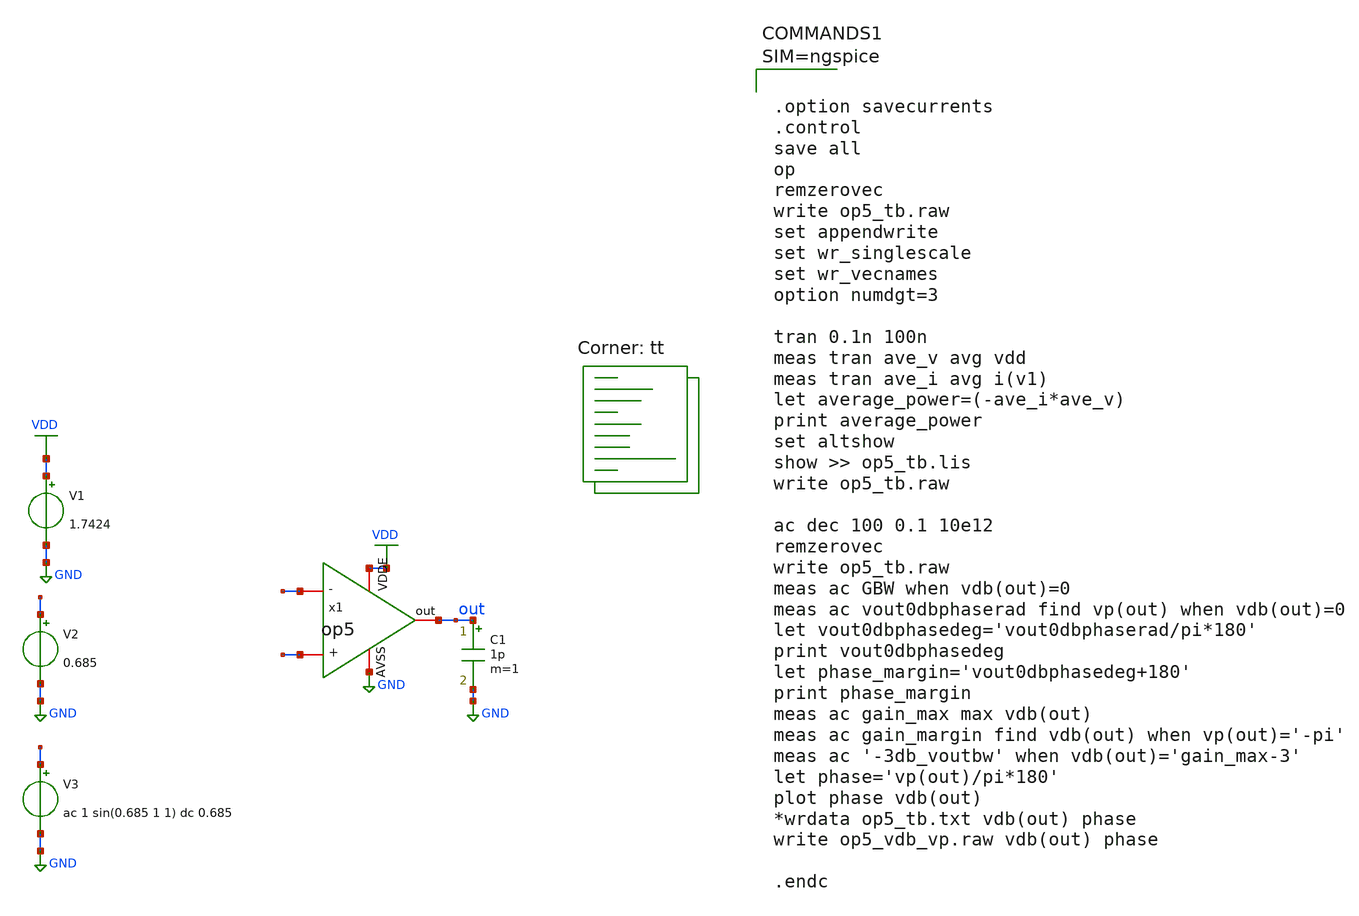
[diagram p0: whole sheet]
** sch_path: xschem/op5_tb.sch
**.subckt op5_tb
V1 VDD GND 1.7424
V2 - GND 0.685
V3 + GND ac 1 sin(0.685 1 1) dc 0.685
C1 out GND 1p m=1
x1 out VDD GND + - op5
**** begin user architecture code



.option savecurrents
.control
save all
op
remzerovec
write op5_tb.raw
set appendwrite
set wr_singlescale
set wr_vecnames
option numdgt=3

tran 0.1n 100n
meas tran ave_v avg vdd
meas tran ave_i avg i(v1)
let average_power=(-ave_i*ave_v)
print average_power
set altshow
show >> op5_tb.lis
write op5_tb.raw

ac dec 100 0.1 10e12
remzerovec
write op5_tb.raw
meas ac GBW when vdb(out)=0
meas ac vout0dbphaserad find vp(out) when vdb(out)=0
let vout0dbphasedeg='vout0dbphaserad/pi*180'
print vout0dbphasedeg
let phase_margin='vout0dbphasedeg+180'
print phase_margin
meas ac gain_max max vdb(out)
meas ac gain_margin find vdb(out) when vp(out)='-pi'
meas ac '-3db_voutbw' when vdb(out)='gain_max-3'
let phase='vp(out)/pi*180'
plot phase vdb(out)
*wrdata op5_tb.txt vdb(out) phase
write op5_vdb_vp.raw vdb(out) phase

.endc



.lib $::SKYWATER_MODELS/sky130.lib.spice tt
**** end user architecture code
**.ends

* expanding   symbol:  op5.sym # of pins=5
** sym_path: xschem/op5.sym
** sch_path: xschem/op5.sch
.subckt op5 out VDDE AVSS + -
*.iopin AVSS
*.iopin -
*.iopin +
*.iopin VDDE
*.iopin out
XM8 net1 net2 VDDE vdde sky130_fd_pr__pfet_01v8 L={L7} W={W7} nf=1 ad='int((nf+1)/2) * W/nf * 0.29' as='int((nf+2)/2) * W/nf * 0.29'
+ pd='2*int((nf+1)/2) * (W/nf + 0.29)' ps='2*int((nf+2)/2) * (W/nf + 0.29)' nrd='0.29 / W' nrs='0.29 / W'
+ sa=0 sb=0 sd=0 mult=2 m=2
XM9 net2 net2 VDDE vdde sky130_fd_pr__pfet_01v8 L={L7} W={W7} nf=1 ad='int((nf+1)/2) * W/nf * 0.29' as='int((nf+2)/2) * W/nf * 0.29'
+ pd='2*int((nf+1)/2) * (W/nf + 0.29)' ps='2*int((nf+2)/2) * (W/nf + 0.29)' nrd='0.29 / W' nrs='0.29 / W'
+ sa=0 sb=0 sd=0 mult=2 m=2
XM5 net3 bias AVSS AVSS sky130_fd_pr__nfet_01v8 L={L6} W={W6} nf=1 ad='int((nf+1)/2) * W/nf * 0.29' as='int((nf+2)/2) * W/nf * 0.29'
+ pd='2*int((nf+1)/2) * (W/nf + 0.29)' ps='2*int((nf+2)/2) * (W/nf + 0.29)' nrd='0.29 / W' nrs='0.29 / W'
+ sa=0 sb=0 sd=0 mult=2 m=2
XM10 out net1 VDDE vdde sky130_fd_pr__pfet_01v8 L={L2} W={W2} nf=1 ad='int((nf+1)/2) * W/nf * 0.29' as='int((nf+2)/2) * W/nf * 0.29'
+ pd='2*int((nf+1)/2) * (W/nf + 0.29)' ps='2*int((nf+2)/2) * (W/nf + 0.29)' nrd='0.29 / W' nrs='0.29 / W'
+ sa=0 sb=0 sd=0 mult=4 m=4
**** begin user architecture code


.include /home/gils/sky130_pdk/share/pdk/sky130A/libs.ref/sky130_fd_pr/spice/sky130_fd_pr__cap_vpp_11p5x11p7_l1m1m2m3_shieldm4.model.spice
**************
*PMOS cms
.param L1=10
.param W1=1

**************
*PMOS current differential
.param L7=10
.param W7=1

**************
*differential Pair
.param L4=13
.param W4=0.9

**************
*NMOS current control
.param L6=20
.param W6=1

**************
*Second Stage
.param L2=10
.param W2=1


**** end user architecture code
XM11 out bias AVSS AVSS sky130_fd_pr__nfet_01v8 L={L6} W={W6} nf=1 ad='int((nf+1)/2) * W/nf * 0.29' as='int((nf+2)/2) * W/nf * 0.29'
+ pd='2*int((nf+1)/2) * (W/nf + 0.29)' ps='2*int((nf+2)/2) * (W/nf + 0.29)' nrd='0.29 / W' nrs='0.29 / W'
+ sa=0 sb=0 sd=0 mult=2 m=2
XM3 net1 + net3 AVSS sky130_fd_pr__nfet_01v8 L={L4} W={W4} nf=1 ad='int((nf+1)/2) * W/nf * 0.29' as='int((nf+2)/2) * W/nf * 0.29'
+ pd='2*int((nf+1)/2) * (W/nf + 0.29)' ps='2*int((nf+2)/2) * (W/nf + 0.29)' nrd='0.29 / W' nrs='0.29 / W'
+ sa=0 sb=0 sd=0 mult=2 m=2
XM1 bias net6 VDDE vdde sky130_fd_pr__pfet_01v8 L={L1} W={W1} nf=1 ad='int((nf+1)/2) * W/nf * 0.29' as='int((nf+2)/2) * W/nf * 0.29'
+ pd='2*int((nf+1)/2) * (W/nf + 0.29)' ps='2*int((nf+2)/2) * (W/nf + 0.29)' nrd='0.29 / W' nrs='0.29 / W'
+ sa=0 sb=0 sd=0 mult=2 m=2
XM2 net6 net6 VDDE vdde sky130_fd_pr__pfet_01v8 L={L1} W={W1} nf=1 ad='int((nf+1)/2) * W/nf * 0.29' as='int((nf+2)/2) * W/nf * 0.29'
+ pd='2*int((nf+1)/2) * (W/nf + 0.29)' ps='2*int((nf+2)/2) * (W/nf + 0.29)' nrd='0.29 / W' nrs='0.29 / W'
+ sa=0 sb=0 sd=0 mult=2 m=2
XM6 net6 bias net7 AVSS sky130_fd_pr__nfet_01v8 L={L6} W={W6} nf=1 ad='int((nf+1)/2) * W/nf * 0.29' as='int((nf+2)/2) * W/nf * 0.29'
+ pd='2*int((nf+1)/2) * (W/nf + 0.29)' ps='2*int((nf+2)/2) * (W/nf + 0.29)' nrd='0.29 / W' nrs='0.29 / W'
+ sa=0 sb=0 sd=0 mult=2 m=2
XM7 bias bias AVSS AVSS sky130_fd_pr__nfet_01v8 L={L6} W={W6} nf=1 ad='int((nf+1)/2) * W/nf * 0.29' as='int((nf+2)/2) * W/nf * 0.29'
+ pd='2*int((nf+1)/2) * (W/nf + 0.29)' ps='2*int((nf+2)/2) * (W/nf + 0.29)' nrd='0.29 / W' nrs='0.29 / W'
+ sa=0 sb=0 sd=0 mult=2 m=2
XR4 net7 net8 AVSS sky130_fd_pr__res_high_po_0p35 L=4.5 mult=2 m=2
XM4 net2 - net3 AVSS sky130_fd_pr__nfet_01v8 L={L4} W={W4} nf=1 ad='int((nf+1)/2) * W/nf * 0.29' as='int((nf+2)/2) * W/nf * 0.29'
+ pd='2*int((nf+1)/2) * (W/nf + 0.29)' ps='2*int((nf+2)/2) * (W/nf + 0.29)' nrd='0.29 / W' nrs='0.29 / W'
+ sa=0 sb=0 sd=0 mult=2 m=2
XR1 net1 net4 AVSS sky130_fd_pr__res_high_po_0p35 L=4.5 mult=2 m=2
XR2 net4 net5 AVSS sky130_fd_pr__res_high_po_0p35 L=4.5 mult=2 m=2
XR9 net8 AVSS AVSS sky130_fd_pr__res_high_po_0p35 L=4.5 mult=2 m=2
XC1 net5 out sky130_fd_pr__cap_mim_m3_1 W=10 L=10 MF=4 m=4
.ends

.GLOBAL VDD
.GLOBAL GND
.end
